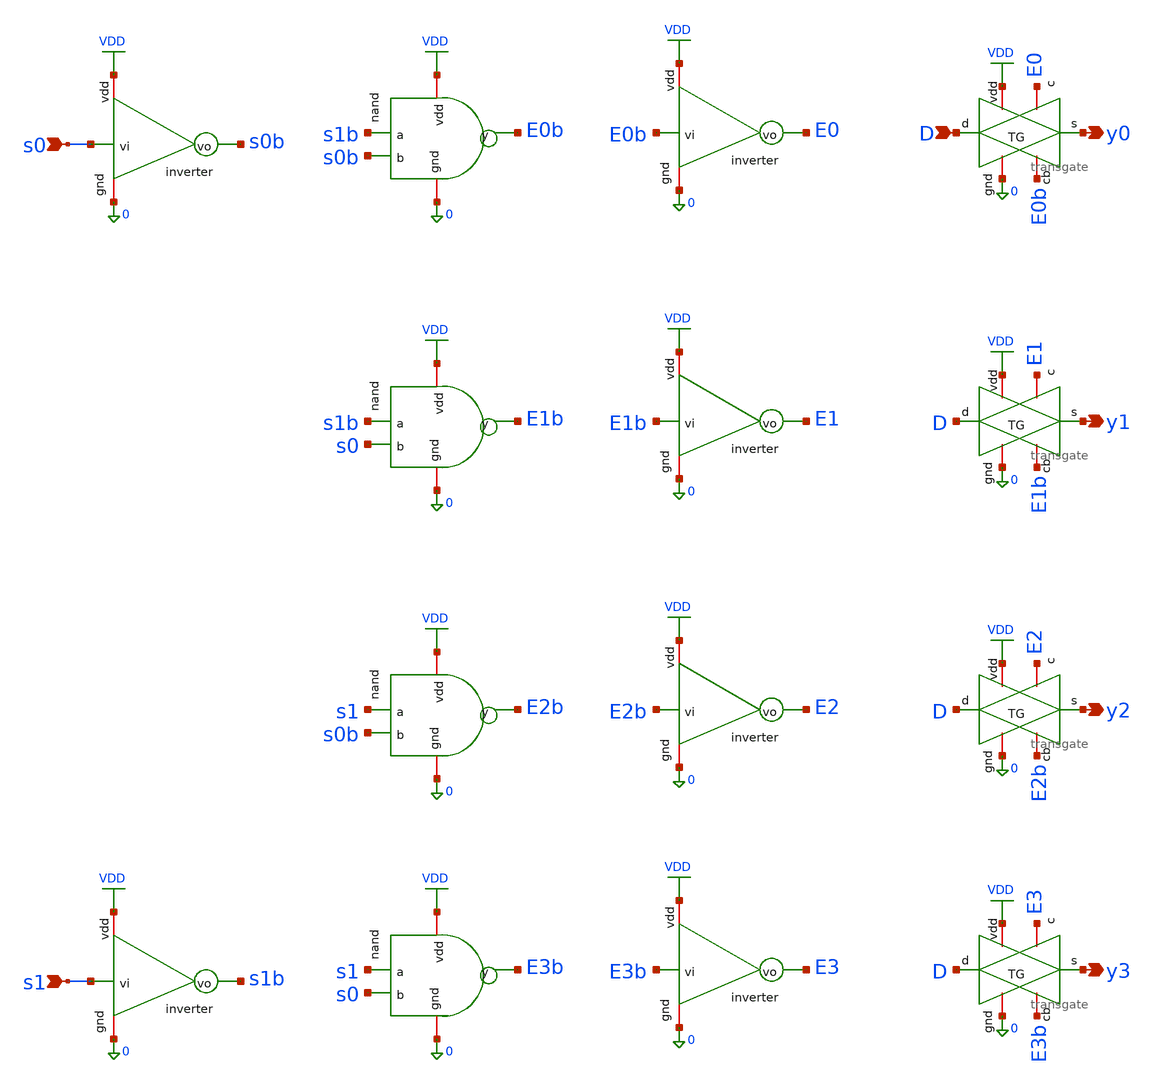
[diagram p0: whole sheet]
** sch_path: src/schematic/DEMUX/demux1to4.sch
**.subckt demux1to4 s0 s1 D y0 y1 y2 y3
*.ipin s0
*.ipin s1
*.ipin D
*.opin y0
*.opin y1
*.opin y2
*.opin y3
x0 VDD s0 s0b 0 inverter
x2 VDD s1 s1b 0 inverter
x3 VDD s1b s0b E0b 0 nand
x4 VDD s1b s0 E1b 0 nand
x5 VDD s1 s0b E2b 0 nand
x6 VDD s1 s0 E3b 0 nand
x7 VDD E0b E0 0 inverter
x8 VDD E1b E1 0 inverter
x9 VDD E2b E2 0 inverter
x10 VDD E3b E3 0 inverter
x11 E0b VDD y0 D 0 E0 transgate
x12 E1b VDD y1 D 0 E1 transgate
x13 E2b VDD y2 D 0 E2 transgate
x14 E3b VDD y3 D 0 E3 transgate
**.ends

* expanding   symbol:  src/schematic/INV/inverter.sym # of pins=4
** sym_path: src/schematic/DEMUX/inverter.sym
** sch_path: src/schematic/DEMUX/inverter.sch
.subckt inverter vdd vi vo gnd
*.ipin vi
*.opin vo
*.iopin vdd
*.iopin gnd
XM1 vo vi vdd vdd pfet_03v3 L=0.28u W=0.22u nf=1 ad='int((nf+1)/2) * W/nf * 0.18u' as='int((nf+2)/2) * W/nf * 0.18u'
+ pd='2*int((nf+1)/2) * (W/nf + 0.18u)' ps='2*int((nf+2)/2) * (W/nf + 0.18u)' nrd='0.18u / W' nrs='0.18u / W'
+ sa=0 sb=0 sd=0 m=1
XM2 vo vi gnd gnd nfet_03v3 L=0.28u W=0.22u nf=1 ad='int((nf+1)/2) * W/nf * 0.18u' as='int((nf+2)/2) * W/nf * 0.18u'
+ pd='2*int((nf+1)/2) * (W/nf + 0.18u)' ps='2*int((nf+2)/2) * (W/nf + 0.18u)' nrd='0.18u / W' nrs='0.18u / W'
+ sa=0 sb=0 sd=0 m=1
.ends


* expanding   symbol:  nand.sym # of pins=5
** sym_path: src/schematic/DEMUX/nand.sym
** sch_path: src/schematic/DEMUX/nand.sch
.subckt nand vdd a b y gnd
*.iopin gnd
*.iopin vdd
*.ipin a
*.ipin b
*.opin y
XM1 y a vdd vdd pfet_03v3 L=0.28u W=0.22u nf=1 ad='int((nf+1)/2) * W/nf * 0.18u' as='int((nf+2)/2) * W/nf * 0.18u'
+ pd='2*int((nf+1)/2) * (W/nf + 0.18u)' ps='2*int((nf+2)/2) * (W/nf + 0.18u)' nrd='0.18u / W' nrs='0.18u / W'
+ sa=0 sb=0 sd=0 m=1
XM2 y b vdd vdd pfet_03v3 L=0.28u W=0.22u nf=1 ad='int((nf+1)/2) * W/nf * 0.18u' as='int((nf+2)/2) * W/nf * 0.18u'
+ pd='2*int((nf+1)/2) * (W/nf + 0.18u)' ps='2*int((nf+2)/2) * (W/nf + 0.18u)' nrd='0.18u / W' nrs='0.18u / W'
+ sa=0 sb=0 sd=0 m=1
XM3 y a net1 gnd nfet_03v3 L=0.28u W=0.22u nf=1 ad='int((nf+1)/2) * W/nf * 0.18u' as='int((nf+2)/2) * W/nf * 0.18u'
+ pd='2*int((nf+1)/2) * (W/nf + 0.18u)' ps='2*int((nf+2)/2) * (W/nf + 0.18u)' nrd='0.18u / W' nrs='0.18u / W'
+ sa=0 sb=0 sd=0 m=1
XM4 net1 b gnd gnd nfet_03v3 L=0.28u W=0.22u nf=1 ad='int((nf+1)/2) * W/nf * 0.18u' as='int((nf+2)/2) * W/nf * 0.18u'
+ pd='2*int((nf+1)/2) * (W/nf + 0.18u)' ps='2*int((nf+2)/2) * (W/nf + 0.18u)' nrd='0.18u / W' nrs='0.18u / W'
+ sa=0 sb=0 sd=0 m=1
.ends


* expanding   symbol:  src/schematic/TG/transgate.sym # of pins=6
** sym_path: src/schematic/DEMUX/transgate.sym
** sch_path: src/schematic/DEMUX/transgate.sch
.subckt transgate cb vdd s d gnd c
*.iopin gnd
*.iopin vdd
*.iopin cb
*.iopin c
*.ipin d
*.opin s
XM1 d c s gnd nfet_03v3 L=0.28u W=0.22u nf=1 ad='int((nf+1)/2) * W/nf * 0.18u' as='int((nf+2)/2) * W/nf * 0.18u'
+ pd='2*int((nf+1)/2) * (W/nf + 0.18u)' ps='2*int((nf+2)/2) * (W/nf + 0.18u)' nrd='0.18u / W' nrs='0.18u / W'
+ sa=0 sb=0 sd=0 m=1
XM2 d cb s vdd pfet_03v3 L=0.28u W=0.22u nf=1 ad='int((nf+1)/2) * W/nf * 0.18u' as='int((nf+2)/2) * W/nf * 0.18u'
+ pd='2*int((nf+1)/2) * (W/nf + 0.18u)' ps='2*int((nf+2)/2) * (W/nf + 0.18u)' nrd='0.18u / W' nrs='0.18u / W'
+ sa=0 sb=0 sd=0 m=1
.ends

.GLOBAL VDD
.end
